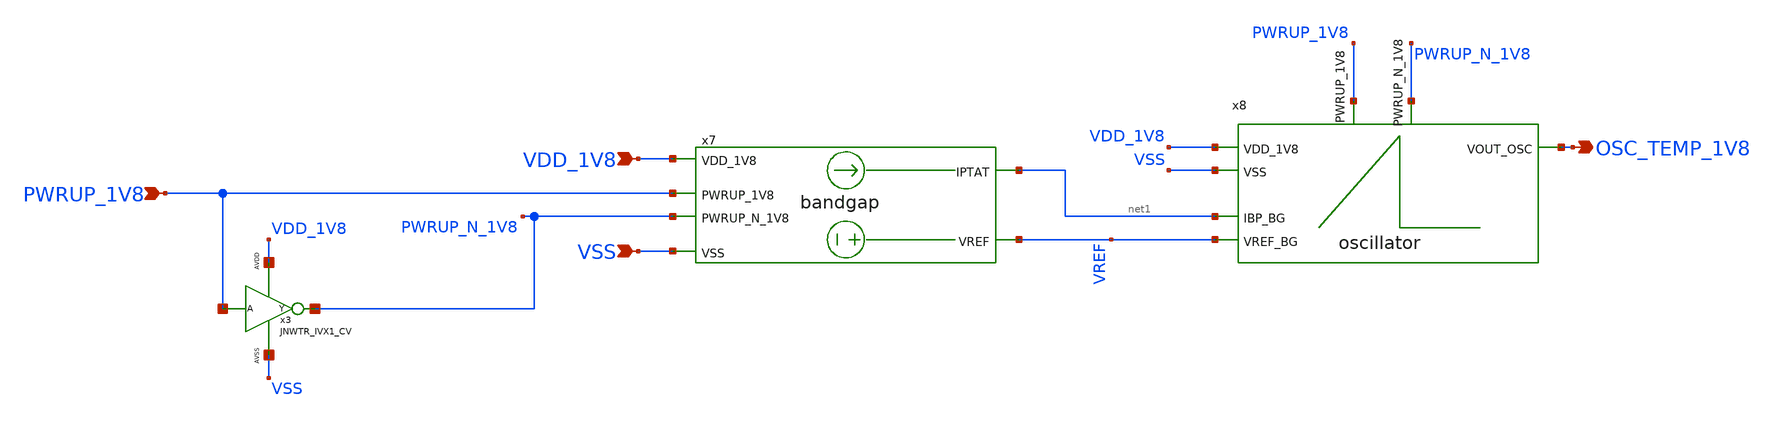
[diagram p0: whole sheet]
** sch_path: design/LELO_GR01_SKY130A/LELO_GR01.sch
**.subckt LELO_GR01 VDD_1V8 VSS PWRUP_1V8 OSC_TEMP_1V8
*.ipin VDD_1V8
*.ipin VSS
*.ipin PWRUP_1V8
*.opin OSC_TEMP_1V8
x7 net1 VREF PWRUP_1V8 VDD_1V8 VSS PWRUP_N_1V8 bandgap
x8 OSC_TEMP_1V8 VDD_1V8 VSS net1 VREF PWRUP_1V8 PWRUP_N_1V8 oscillator
x3 PWRUP_1V8 PWRUP_N_1V8 VDD_1V8 VSS JNWTR_IVX1_CV
**.ends
.end
